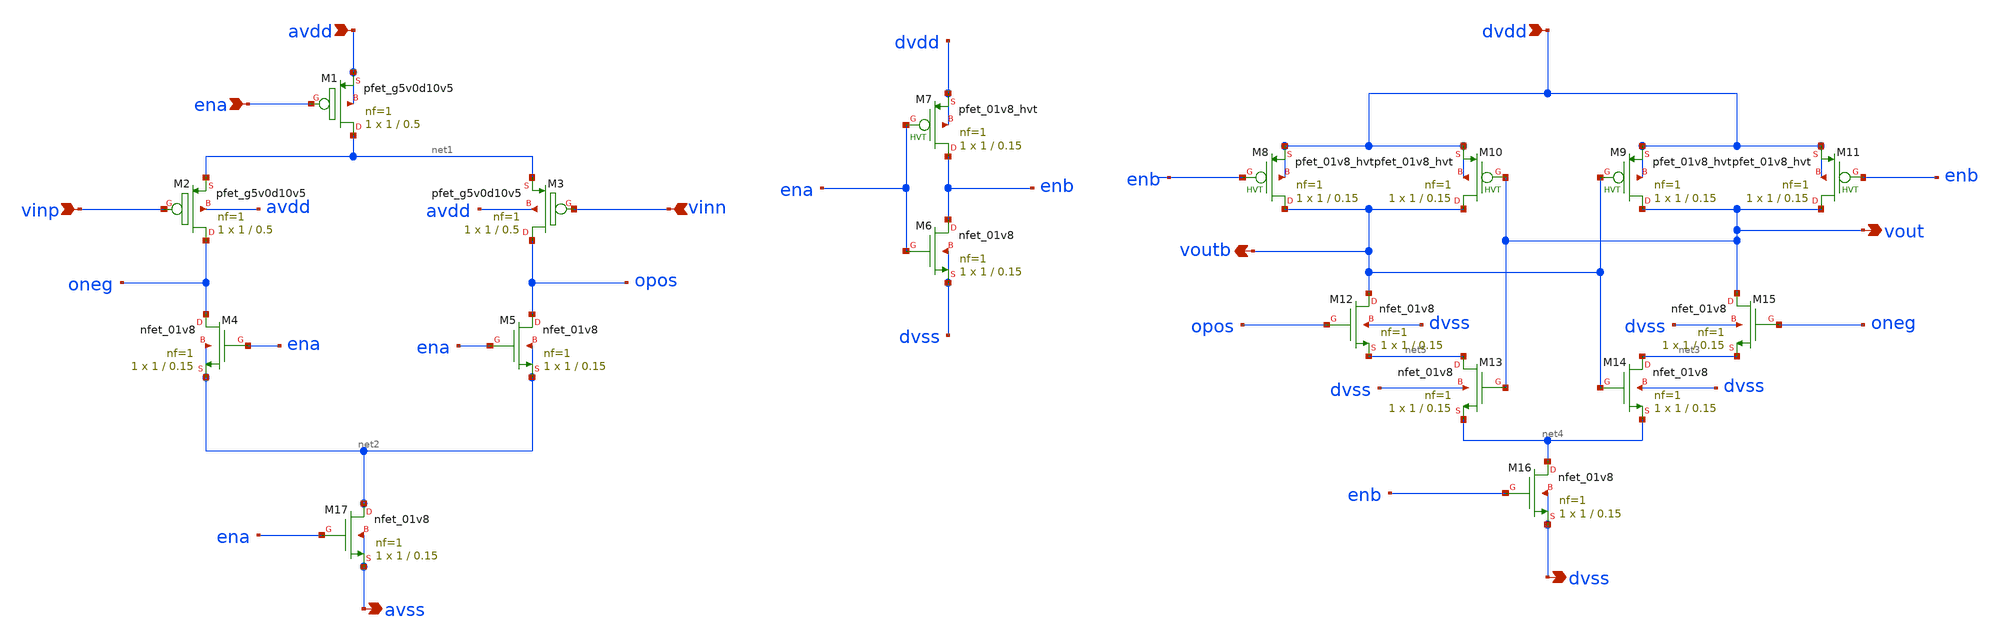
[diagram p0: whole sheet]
** sch_path: cace/sky130_icrg_ip__ulpcomp.sch
**.subckt sky130_icrg_ip__ulpcomp ena vinp vinn avss avdd dvdd dvss vout voutb
*.ipin ena
*.ipin vinp
*.ipin vinn
*.opin avss
*.ipin avdd
*.ipin dvdd
*.opin dvss
*.opin vout
*.opin voutb
XM4 oneg ena net2 net2 sky130_fd_pr__nfet_01v8 L=0.15 W=1 nf=1 ad='int((nf+1)/2) * W/nf * 0.29' as='int((nf+2)/2) * W/nf * 0.29'
+ pd='2*int((nf+1)/2) * (W/nf + 0.29)' ps='2*int((nf+2)/2) * (W/nf + 0.29)' nrd='0.29 / W' nrs='0.29 / W'
+ sa=0 sb=0 sd=0 mult=1 m=1
XM5 opos ena net2 net2 sky130_fd_pr__nfet_01v8 L=0.15 W=1 nf=1 ad='int((nf+1)/2) * W/nf * 0.29' as='int((nf+2)/2) * W/nf * 0.29'
+ pd='2*int((nf+1)/2) * (W/nf + 0.29)' ps='2*int((nf+2)/2) * (W/nf + 0.29)' nrd='0.29 / W' nrs='0.29 / W'
+ sa=0 sb=0 sd=0 mult=1 m=1
XM6 enb ena dvss dvss sky130_fd_pr__nfet_01v8 L=0.15 W=1 nf=1 ad='int((nf+1)/2) * W/nf * 0.29' as='int((nf+2)/2) * W/nf * 0.29'
+ pd='2*int((nf+1)/2) * (W/nf + 0.29)' ps='2*int((nf+2)/2) * (W/nf + 0.29)' nrd='0.29 / W' nrs='0.29 / W'
+ sa=0 sb=0 sd=0 mult=1 m=1
XM12 voutb opos net5 dvss sky130_fd_pr__nfet_01v8 L=0.15 W=1 nf=1 ad='int((nf+1)/2) * W/nf * 0.29' as='int((nf+2)/2) * W/nf * 0.29'
+ pd='2*int((nf+1)/2) * (W/nf + 0.29)' ps='2*int((nf+2)/2) * (W/nf + 0.29)' nrd='0.29 / W' nrs='0.29 / W'
+ sa=0 sb=0 sd=0 mult=1 m=1
XM13 net5 vout net4 dvss sky130_fd_pr__nfet_01v8 L=0.15 W=1 nf=1 ad='int((nf+1)/2) * W/nf * 0.29' as='int((nf+2)/2) * W/nf * 0.29'
+ pd='2*int((nf+1)/2) * (W/nf + 0.29)' ps='2*int((nf+2)/2) * (W/nf + 0.29)' nrd='0.29 / W' nrs='0.29 / W'
+ sa=0 sb=0 sd=0 mult=1 m=1
XM14 net3 voutb net4 dvss sky130_fd_pr__nfet_01v8 L=0.15 W=1 nf=1 ad='int((nf+1)/2) * W/nf * 0.29' as='int((nf+2)/2) * W/nf * 0.29'
+ pd='2*int((nf+1)/2) * (W/nf + 0.29)' ps='2*int((nf+2)/2) * (W/nf + 0.29)' nrd='0.29 / W' nrs='0.29 / W'
+ sa=0 sb=0 sd=0 mult=1 m=1
XM15 vout oneg net3 dvss sky130_fd_pr__nfet_01v8 L=0.15 W=1 nf=1 ad='int((nf+1)/2) * W/nf * 0.29' as='int((nf+2)/2) * W/nf * 0.29'
+ pd='2*int((nf+1)/2) * (W/nf + 0.29)' ps='2*int((nf+2)/2) * (W/nf + 0.29)' nrd='0.29 / W' nrs='0.29 / W'
+ sa=0 sb=0 sd=0 mult=1 m=1
XM16 net4 enb dvss dvss sky130_fd_pr__nfet_01v8 L=0.15 W=1 nf=1 ad='int((nf+1)/2) * W/nf * 0.29' as='int((nf+2)/2) * W/nf * 0.29'
+ pd='2*int((nf+1)/2) * (W/nf + 0.29)' ps='2*int((nf+2)/2) * (W/nf + 0.29)' nrd='0.29 / W' nrs='0.29 / W'
+ sa=0 sb=0 sd=0 mult=1 m=1
XM1 net1 ena avdd avdd sky130_fd_pr__pfet_g5v0d10v5 L=0.5 W=1 nf=1 ad='int((nf+1)/2) * W/nf * 0.29' as='int((nf+2)/2) * W/nf * 0.29'
+ pd='2*int((nf+1)/2) * (W/nf + 0.29)' ps='2*int((nf+2)/2) * (W/nf + 0.29)' nrd='0.29 / W' nrs='0.29 / W'
+ sa=0 sb=0 sd=0 mult=1 m=1
XM2 oneg vinp net1 avdd sky130_fd_pr__pfet_g5v0d10v5 L=0.5 W=1 nf=1 ad='int((nf+1)/2) * W/nf * 0.29'
+ as='int((nf+2)/2) * W/nf * 0.29' pd='2*int((nf+1)/2) * (W/nf + 0.29)' ps='2*int((nf+2)/2) * (W/nf + 0.29)'
+ nrd='0.29 / W' nrs='0.29 / W' sa=0 sb=0 sd=0 mult=1 m=1
XM3 opos vinn net1 avdd sky130_fd_pr__pfet_g5v0d10v5 L=0.5 W=1 nf=1 ad='int((nf+1)/2) * W/nf * 0.29'
+ as='int((nf+2)/2) * W/nf * 0.29' pd='2*int((nf+1)/2) * (W/nf + 0.29)' ps='2*int((nf+2)/2) * (W/nf + 0.29)'
+ nrd='0.29 / W' nrs='0.29 / W' sa=0 sb=0 sd=0 mult=1 m=1
XM7 enb ena dvdd dvdd sky130_fd_pr__pfet_01v8_hvt L=0.15 W=1 nf=1 ad='int((nf+1)/2) * W/nf * 0.29' as='int((nf+2)/2) * W/nf * 0.29'
+ pd='2*int((nf+1)/2) * (W/nf + 0.29)' ps='2*int((nf+2)/2) * (W/nf + 0.29)' nrd='0.29 / W' nrs='0.29 / W'
+ sa=0 sb=0 sd=0 mult=1 m=1
XM17 net2 ena avss avss sky130_fd_pr__nfet_01v8 L=0.15 W=1 nf=1 ad='int((nf+1)/2) * W/nf * 0.29' as='int((nf+2)/2) * W/nf * 0.29'
+ pd='2*int((nf+1)/2) * (W/nf + 0.29)' ps='2*int((nf+2)/2) * (W/nf + 0.29)' nrd='0.29 / W' nrs='0.29 / W'
+ sa=0 sb=0 sd=0 mult=1 m=1
XM8 voutb enb dvdd dvdd sky130_fd_pr__pfet_01v8_hvt L=0.15 W=1 nf=1 ad='int((nf+1)/2) * W/nf * 0.29'
+ as='int((nf+2)/2) * W/nf * 0.29' pd='2*int((nf+1)/2) * (W/nf + 0.29)' ps='2*int((nf+2)/2) * (W/nf + 0.29)'
+ nrd='0.29 / W' nrs='0.29 / W' sa=0 sb=0 sd=0 mult=1 m=1
XM9 vout voutb dvdd dvdd sky130_fd_pr__pfet_01v8_hvt L=0.15 W=1 nf=1 ad='int((nf+1)/2) * W/nf * 0.29'
+ as='int((nf+2)/2) * W/nf * 0.29' pd='2*int((nf+1)/2) * (W/nf + 0.29)' ps='2*int((nf+2)/2) * (W/nf + 0.29)'
+ nrd='0.29 / W' nrs='0.29 / W' sa=0 sb=0 sd=0 mult=1 m=1
XM10 voutb vout dvdd dvdd sky130_fd_pr__pfet_01v8_hvt L=0.15 W=1 nf=1 ad='int((nf+1)/2) * W/nf * 0.29'
+ as='int((nf+2)/2) * W/nf * 0.29' pd='2*int((nf+1)/2) * (W/nf + 0.29)' ps='2*int((nf+2)/2) * (W/nf + 0.29)'
+ nrd='0.29 / W' nrs='0.29 / W' sa=0 sb=0 sd=0 mult=1 m=1
XM11 vout enb dvdd dvdd sky130_fd_pr__pfet_01v8_hvt L=0.15 W=1 nf=1 ad='int((nf+1)/2) * W/nf * 0.29'
+ as='int((nf+2)/2) * W/nf * 0.29' pd='2*int((nf+1)/2) * (W/nf + 0.29)' ps='2*int((nf+2)/2) * (W/nf + 0.29)'
+ nrd='0.29 / W' nrs='0.29 / W' sa=0 sb=0 sd=0 mult=1 m=1
**.ends
.end
